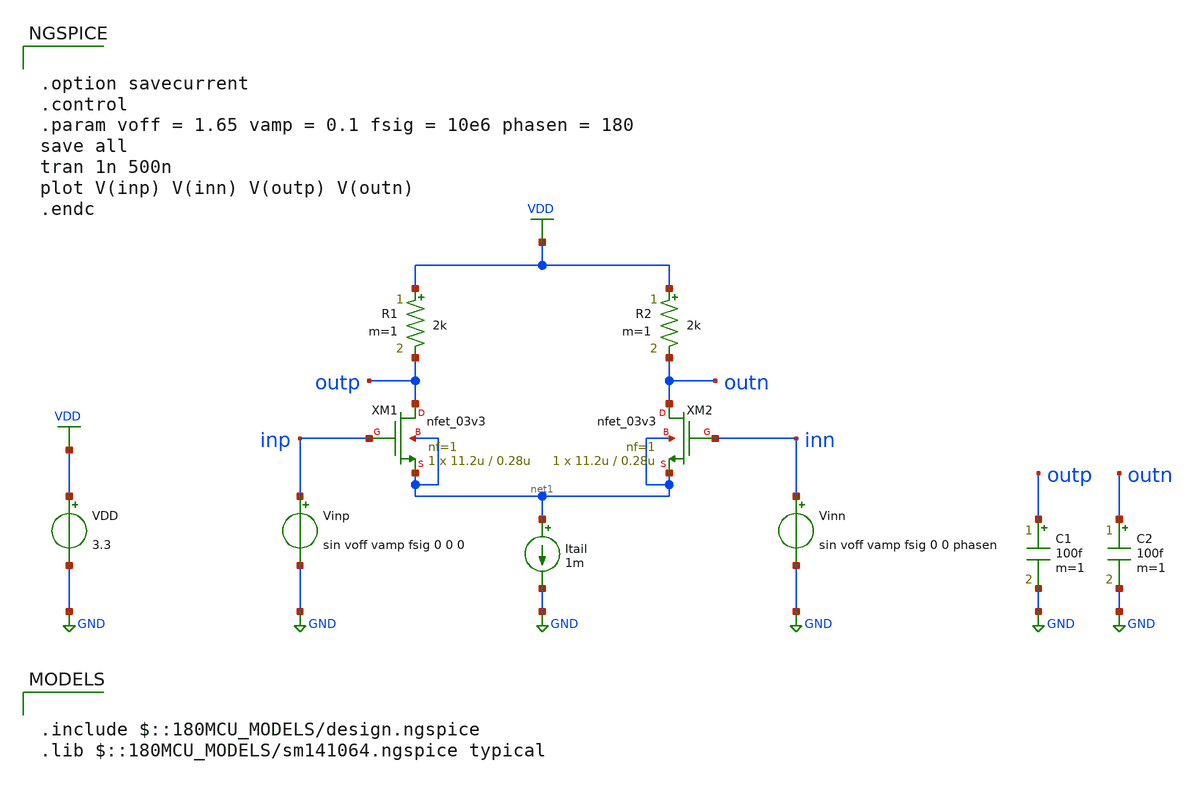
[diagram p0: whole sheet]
** sch_path: fifty_nifty/08_diff_tran.sch
**.subckt 08_diff_tran
XM1 outp inp net1 net1 nfet_03v3 L=0.28u W=11.2u nf=1 ad='int((nf+1)/2) * W/nf * 0.18u' as='int((nf+2)/2) * W/nf * 0.18u'
+ pd='2*int((nf+1)/2) * (W/nf + 0.18u)' ps='2*int((nf+2)/2) * (W/nf + 0.18u)' nrd='0.18u / W' nrs='0.18u / W'
+ sa=0 sb=0 sd=0 m=1
VDD VDD GND 3.3
XM2 outn inn net1 net1 nfet_03v3 L=0.28u W=11.2u nf=1 ad='int((nf+1)/2) * W/nf * 0.18u' as='int((nf+2)/2) * W/nf * 0.18u'
+ pd='2*int((nf+1)/2) * (W/nf + 0.18u)' ps='2*int((nf+2)/2) * (W/nf + 0.18u)' nrd='0.18u / W' nrs='0.18u / W'
+ sa=0 sb=0 sd=0 m=1
Itail net1 GND 1m
Vinp inp GND sin voff vamp fsig 0 0 0
R1 VDD outp 2k m=1
R2 VDD outn 2k m=1
Vinn inn GND sin voff vamp fsig 0 0 phasen
C1 outp GND 100f m=1
C2 outn GND 100f m=1
**** begin user architecture code

.option savecurrent
.control
.param voff = 1.65 vamp = 0.1 fsig = 10e6 phasen = 180
save all
tran 1n 500n
plot V(inp) V(inn) V(outp) V(outn)
.endc


.include $::180MCU_MODELS/design.ngspice
.lib $::180MCU_MODELS/sm141064.ngspice typical

**** end user architecture code
**.ends
.GLOBAL GND
.GLOBAL VDD
.end
